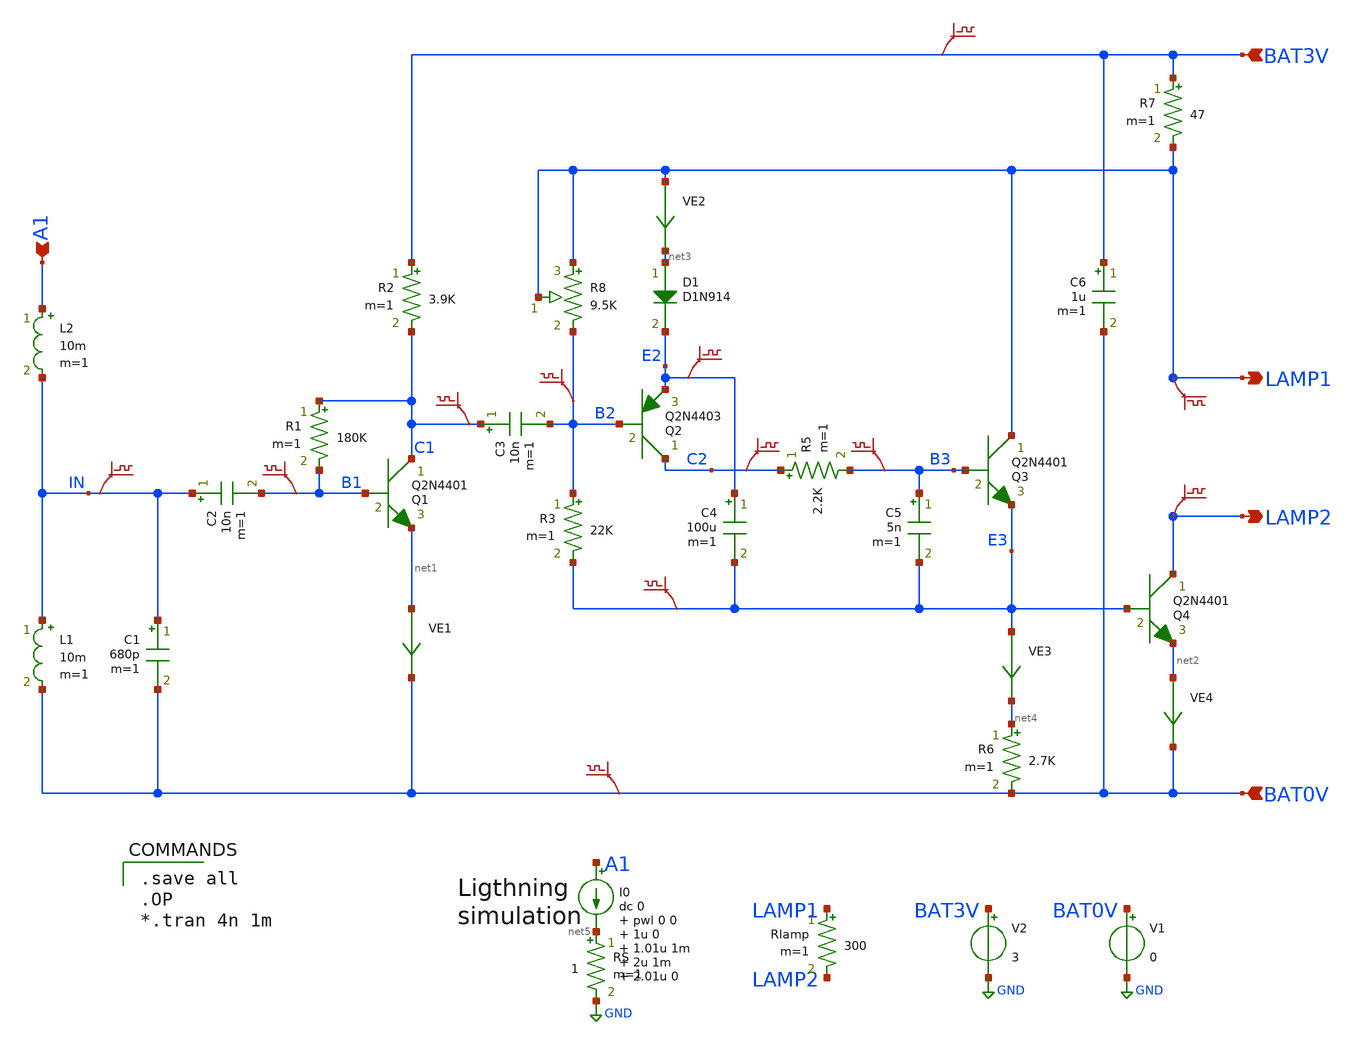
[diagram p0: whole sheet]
** sch_path: tests/test_sweep_diff/examples/lightning/schematic/lightning.sch
* Copyright (C) 1998-2024 Stefan Frederik Schippers
* This program is free software; you can redistribute it and/or modify
* it under the terms of the GNU General Public License as published by
* the Free Software Foundation; either version 2 of the License, or
* (at your option) any later version.
* This program is distributed in the hope that it will be useful,
* but WITHOUT ANY WARRANTY; without even the implied warranty of
* MERCHANTABILITY or FITNESS FOR A PARTICULAR PURPOSE.  See the
* GNU General Public License for more details.
* You should have received a copy of the GNU General Public License
* along with this program; if not, write to the Free Software
**.subckt lightning A1 BAT3V BAT0V LAMP1 LAMP2
*.ipin A1
*.ipin BAT3V
*.ipin BAT0V
*.opin LAMP1
*.opin LAMP2
L2 A1 IN 10m m=1
L1 IN BAT0V 10m m=1
C2 IN B1 10n m=1
C1 IN BAT0V 680p m=1
Q1 C1 B1 net1 Q2N4401 area=1 m=1
R2 BAT3V C1 3.9K m=1
R1 C1 B1 180K m=1
C3 C1 B2 10n m=1
Q2 C2 B2 E2 Q2N4403 area=1 m=1
D1 net3 E2 D1N914 area=1
R3 B2 E3 22K m=1
C4 E2 E3 100u m=1
R5 C2 B3 2.2K m=1
C5 B3 E3 5n m=1
Q3 LAMP1 B3 E3 Q2N4401 area=1 m=1
R6 net4 BAT0V 2.7K m=1
Q4 LAMP2 E3 net2 Q2N4401 area=1 m=1
C6 BAT3V BAT0V 1u m=1
R7 BAT3V LAMP1 47 m=1
R8 LAMP1 B2 9.5K m=1
.save v(bat3v)
.save v(in)
.save v(b1)
.save v(e3)
.save v(b3)
.save v(b2)
.save v(bat0v)
V1 BAT0V GND 0
V2 BAT3V GND 3
.save v(c1)
.save v(c2)
.save v(lamp2)
.save v(lamp1)
Rlamp LAMP1 LAMP2 300 m=1
.save v(e2)
I0 A1 net5 dc 0 pwl 0 0 1u 0 1.01u 1m 2u 1m 2.01u 0
RS net5 GND 1 m=1
VE1 net1 BAT0V 0
.save i(ve1)
VE4 net2 BAT0V 0
.save i(ve4)
VE2 LAMP1 net3 0
.save i(ve2)
VE3 E3 net4 0
.save i(ve3)
**** begin user architecture code


** you need to get the spice models for Q2N4401, Q2N4403 and D1N914
** and put them in file referenced below.
.include models_lightning.txt



.save all
.OP
*.tran 4n 1m


**** end user architecture code
**.ends
.GLOBAL GND
.end
